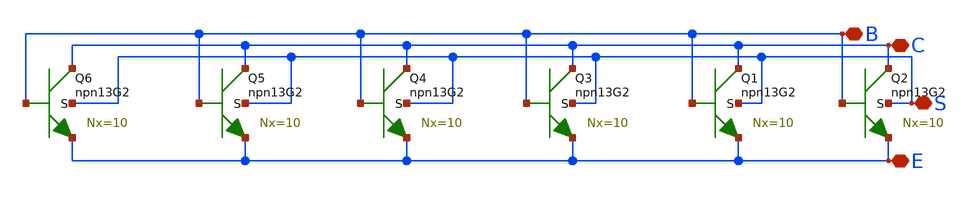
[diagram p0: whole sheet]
** sch_path: GPS_LNA/design_data/lvs/parts/npn_60.sch
**.subckt npn_60 S E C B
*.iopin S
*.iopin E
*.iopin C
*.iopin B
XQ1 C B E S npn13G2 Nx=10 mm_ok=1
XQ2 C B E S npn13G2 Nx=10 mm_ok=1
XQ3 C B E S npn13G2 Nx=10 mm_ok=1
XQ4 C B E S npn13G2 Nx=10 mm_ok=1
XQ5 C B E S npn13G2 Nx=10 mm_ok=1
XQ6 C B E S npn13G2 Nx=10 mm_ok=1
**.ends
.end
